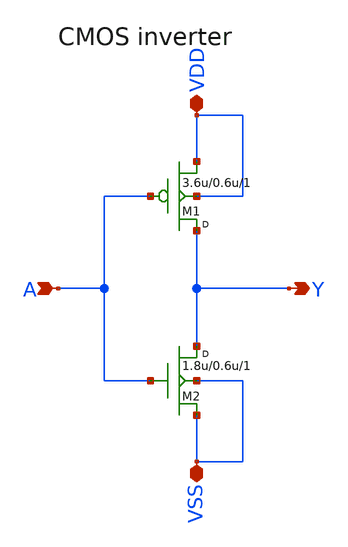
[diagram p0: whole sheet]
** sch_path: sch/inv.sch
**.subckt inv A Y VDD VSS
*.ipin A
*.opin Y
*.iopin VDD
*.iopin VSS
M1 Y A VDD VDD pfet w=3.6u l=0.6u m=1
M2 Y A VSS VSS nfet w=1.8u l=0.6u m=1
**.ends
.end
